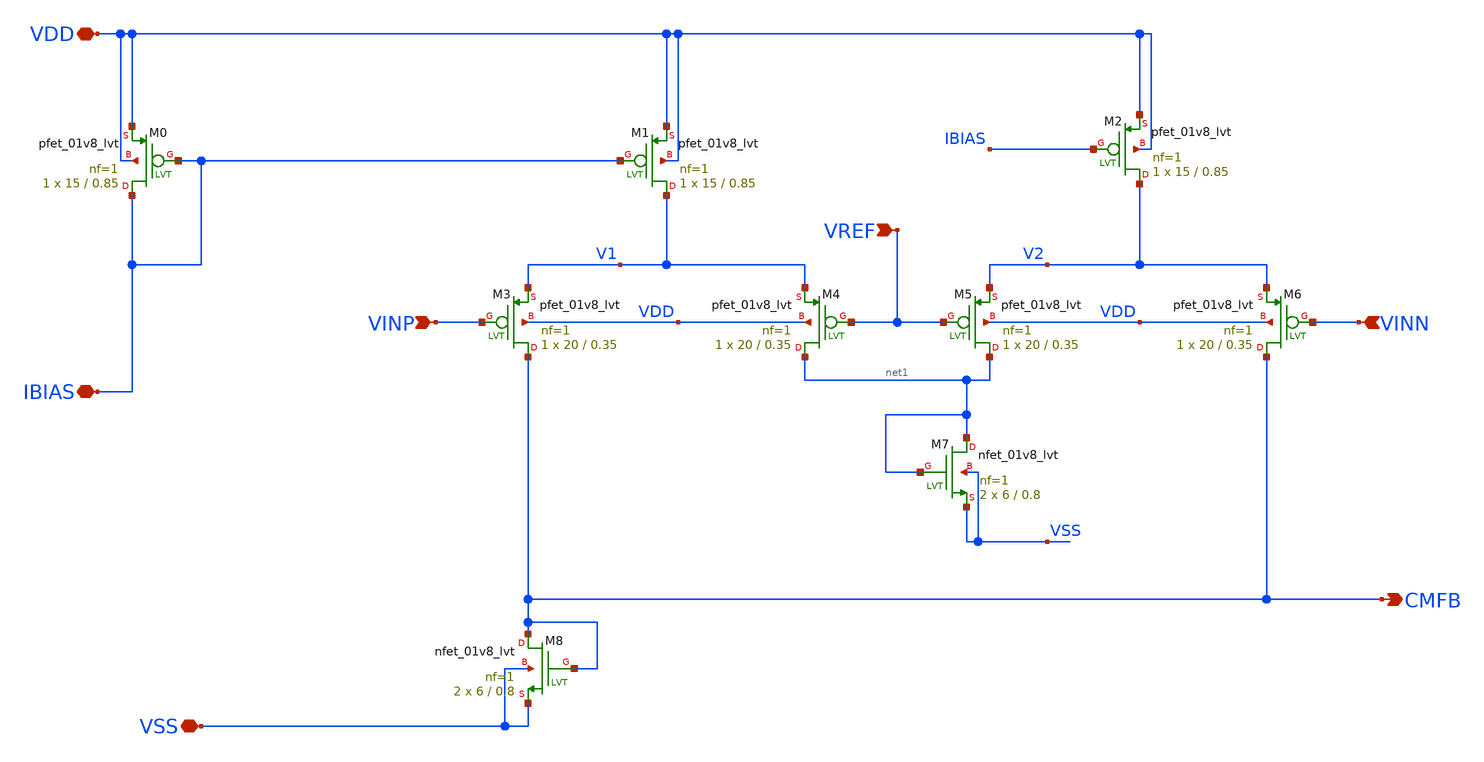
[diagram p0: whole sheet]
** sch_path: Differential_OTA_Telescopic_IHP/OTA_Telescopic_CMFB.sch
**.subckt OTA_Telescopic_CMFB VDD VSS CMFB VREF IBIAS VINP VINN
*.iopin VDD
*.iopin VSS
*.opin CMFB
*.ipin VREF
*.iopin IBIAS
*.ipin VINP
*.ipin VINN
XM0 IBIAS IBIAS VDD VDD sky130_fd_pr__pfet_01v8_lvt L=0.85 W=15 nf=1 ad='int((nf+1)/2) * W/nf * 0.29'
+ as='int((nf+2)/2) * W/nf * 0.29' pd='2*int((nf+1)/2) * (W/nf + 0.29)' ps='2*int((nf+2)/2) * (W/nf + 0.29)'
+ nrd='0.29 / W' nrs='0.29 / W' sa=0 sb=0 sd=0 mult=1 m=1
XM7 net1 net1 VSS VSS sky130_fd_pr__nfet_01v8_lvt L=0.8 W=6 nf=1 ad='int((nf+1)/2) * W/nf * 0.29' as='int((nf+2)/2) * W/nf * 0.29'
+ pd='2*int((nf+1)/2) * (W/nf + 0.29)' ps='2*int((nf+2)/2) * (W/nf + 0.29)' nrd='0.29 / W' nrs='0.29 / W'
+ sa=0 sb=0 sd=0 mult=2 m=2
XM4 net1 VREF V1 VDD sky130_fd_pr__pfet_01v8_lvt L=0.35 W=20 nf=1 ad='int((nf+1)/2) * W/nf * 0.29' as='int((nf+2)/2) * W/nf * 0.29'
+ pd='2*int((nf+1)/2) * (W/nf + 0.29)' ps='2*int((nf+2)/2) * (W/nf + 0.29)' nrd='0.29 / W' nrs='0.29 / W'
+ sa=0 sb=0 sd=0 mult=1 m=1
XM5 net1 VREF V2 VDD sky130_fd_pr__pfet_01v8_lvt L=0.35 W=20 nf=1 ad='int((nf+1)/2) * W/nf * 0.29' as='int((nf+2)/2) * W/nf * 0.29'
+ pd='2*int((nf+1)/2) * (W/nf + 0.29)' ps='2*int((nf+2)/2) * (W/nf + 0.29)' nrd='0.29 / W' nrs='0.29 / W'
+ sa=0 sb=0 sd=0 mult=1 m=1
XM3 CMFB VINP V1 VDD sky130_fd_pr__pfet_01v8_lvt L=0.35 W=20 nf=1 ad='int((nf+1)/2) * W/nf * 0.29' as='int((nf+2)/2) * W/nf * 0.29'
+ pd='2*int((nf+1)/2) * (W/nf + 0.29)' ps='2*int((nf+2)/2) * (W/nf + 0.29)' nrd='0.29 / W' nrs='0.29 / W'
+ sa=0 sb=0 sd=0 mult=1 m=1
XM6 CMFB VINN V2 VDD sky130_fd_pr__pfet_01v8_lvt L=0.35 W=20 nf=1 ad='int((nf+1)/2) * W/nf * 0.29' as='int((nf+2)/2) * W/nf * 0.29'
+ pd='2*int((nf+1)/2) * (W/nf + 0.29)' ps='2*int((nf+2)/2) * (W/nf + 0.29)' nrd='0.29 / W' nrs='0.29 / W'
+ sa=0 sb=0 sd=0 mult=1 m=1
XM1 V1 IBIAS VDD VDD sky130_fd_pr__pfet_01v8_lvt L=0.85 W=15 nf=1 ad='int((nf+1)/2) * W/nf * 0.29' as='int((nf+2)/2) * W/nf * 0.29'
+ pd='2*int((nf+1)/2) * (W/nf + 0.29)' ps='2*int((nf+2)/2) * (W/nf + 0.29)' nrd='0.29 / W' nrs='0.29 / W'
+ sa=0 sb=0 sd=0 mult=1 m=1
XM2 V2 IBIAS VDD VDD sky130_fd_pr__pfet_01v8_lvt L=0.85 W=15 nf=1 ad='int((nf+1)/2) * W/nf * 0.29' as='int((nf+2)/2) * W/nf * 0.29'
+ pd='2*int((nf+1)/2) * (W/nf + 0.29)' ps='2*int((nf+2)/2) * (W/nf + 0.29)' nrd='0.29 / W' nrs='0.29 / W'
+ sa=0 sb=0 sd=0 mult=1 m=1
XM8 CMFB CMFB VSS VSS sky130_fd_pr__nfet_01v8_lvt L=0.8 W=6 nf=1 ad='int((nf+1)/2) * W/nf * 0.29' as='int((nf+2)/2) * W/nf * 0.29'
+ pd='2*int((nf+1)/2) * (W/nf + 0.29)' ps='2*int((nf+2)/2) * (W/nf + 0.29)' nrd='0.29 / W' nrs='0.29 / W'
+ sa=0 sb=0 sd=0 mult=2 m=2
**.ends
.end
